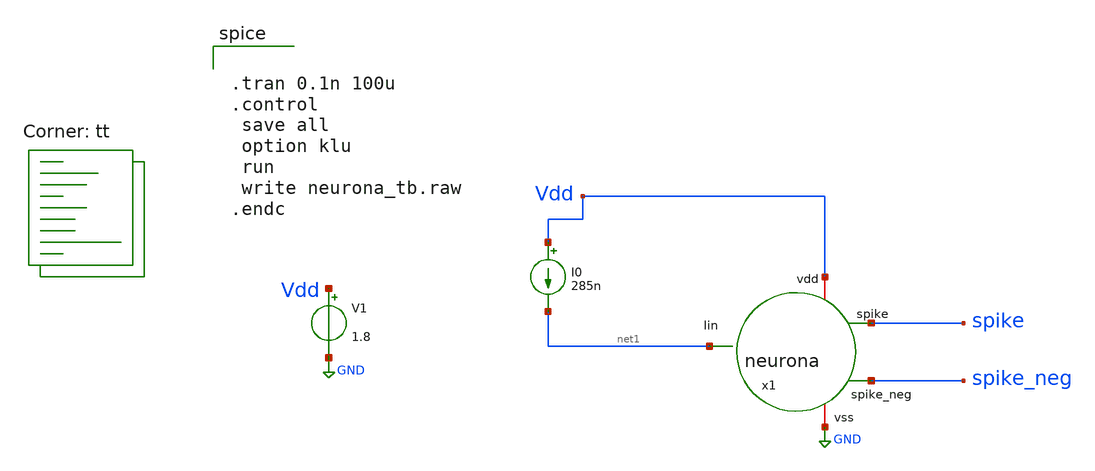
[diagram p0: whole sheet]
** sch_path: designs/libs/snn_analog/lif/sch/neurona_tb.sch
**.subckt neurona_tb
V1 Vdd GND 1.8
I0 Vdd net1 285n
x1 net1 Vdd GND spike spike_neg neurona
**** begin user architecture code


.tran 0.1n 100u
.control
 save all
 option klu
 run
 write neurona_tb.raw
.endc

.lib $::SKYWATER_MODELS/sky130.lib.spice tt
**** end user architecture code
**.ends

* expanding   symbol:  libs/snn_analog/lif/sch/neurona.sym # of pins=5
** sym_path: designs/libs/snn_analog/lif/sch/neurona.sym
** sch_path: designs/libs/snn_analog/lif/sch/neurona.sch
.subckt neurona Iin vdd vss spike spike_neg
*.iopin vdd
*.iopin vss
*.ipin Iin
*.opin spike
*.opin spike_neg
XM2 spike_neg Iin vss vss sky130_fd_pr__nfet_01v8 L=0.28 W=0.5 nf=1 ad='int((1 + 1)/2) * 0.5 / 1 * 0.29'
+ as='int((1 + 2)/2) * 0.5 / 1 * 0.29' pd='2*int((1 + 1)/2) * (0.5 / 1 + 0.29)' ps='2*int((1 + 2)/2) * (0.5 / 1 + 0.29)'
+ nrd='0.29 / 0.5 ' nrs='0.29 / 0.5 ' sa=0 sb=0 sd=0 mult=1 m=1
XM1 spike_neg Iin vdd vdd sky130_fd_pr__pfet_01v8 L=0.28 W=0.5 nf=1 ad='int((1 + 1)/2) * 0.5 / 1 * 0.29'
+ as='int((1 + 2)/2) * 0.5 / 1 * 0.29' pd='2*int((1 + 1)/2) * (0.5 / 1 + 0.29)' ps='2*int((1 + 2)/2) * (0.5 / 1 + 0.29)'
+ nrd='0.29 / 0.5 ' nrs='0.29 / 0.5 ' sa=0 sb=0 sd=0 mult=1 m=1
XM3 spike/reset spike_neg vdd vdd sky130_fd_pr__pfet_01v8 L=0.28 W=0.5 nf=1 ad='int((1 + 1)/2) * 0.5 / 1 * 0.29'
+ as='int((1 + 2)/2) * 0.5 / 1 * 0.29' pd='2*int((1 + 1)/2) * (0.5 / 1 + 0.29)' ps='2*int((1 + 2)/2) * (0.5 / 1 + 0.29)'
+ nrd='0.29 / 0.5 ' nrs='0.29 / 0.5 ' sa=0 sb=0 sd=0 mult=1 m=1
XM4 spike/reset spike_neg vss vss sky130_fd_pr__nfet_01v8 L=0.28 W=0.5 nf=1 ad='int((1 + 1)/2) * 0.5 / 1 * 0.29'
+ as='int((1 + 2)/2) * 0.5 / 1 * 0.29' pd='2*int((1 + 1)/2) * (0.5 / 1 + 0.29)' ps='2*int((1 + 2)/2) * (0.5 / 1 + 0.29)'
+ nrd='0.29 / 0.5 ' nrs='0.29 / 0.5 ' sa=0 sb=0 sd=0 mult=1 m=1
XM5 Iin spike/reset vss vss sky130_fd_pr__nfet_01v8 L=20 W=3 nf=1 ad='int((1 + 1)/2) * 3 / 1 * 0.29'
+ as='int((1 + 2)/2) * 3 / 1 * 0.29' pd='2*int((1 + 1)/2) * (3 / 1 + 0.29)' ps='2*int((1 + 2)/2) * (3 / 1 + 0.29)'
+ nrd='0.29 / 3 ' nrs='0.29 / 3 ' sa=0 sb=0 sd=0 mult=1 m=1
XM6 spike spike_neg vdd vdd sky130_fd_pr__pfet_01v8 L=0.28 W=0.5 nf=1 ad='int((1 + 1)/2) * 0.5 / 1 * 0.29'
+ as='int((1 + 2)/2) * 0.5 / 1 * 0.29' pd='2*int((1 + 1)/2) * (0.5 / 1 + 0.29)' ps='2*int((1 + 2)/2) * (0.5 / 1 + 0.29)'
+ nrd='0.29 / 0.5 ' nrs='0.29 / 0.5 ' sa=0 sb=0 sd=0 mult=1 m=1
XM7 spike spike_neg vss vss sky130_fd_pr__nfet_01v8 L=0.28 W=0.5 nf=1 ad='int((1 + 1)/2) * 0.5 / 1 * 0.29'
+ as='int((1 + 2)/2) * 0.5 / 1 * 0.29' pd='2*int((1 + 1)/2) * (0.5 / 1 + 0.29)' ps='2*int((1 + 2)/2) * (0.5 / 1 + 0.29)'
+ nrd='0.29 / 0.5 ' nrs='0.29 / 0.5 ' sa=0 sb=0 sd=0 mult=1 m=1
XC1 Iin vss sky130_fd_pr__cap_mim_m3_1 W=16.2 L=6.2 MF=1 m=1
.ends

.GLOBAL GND
.end
